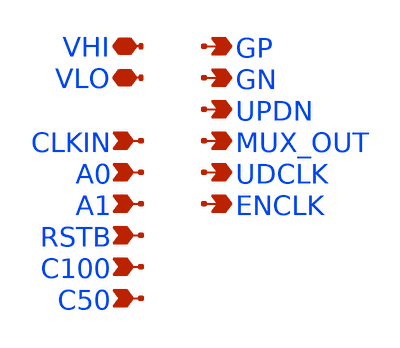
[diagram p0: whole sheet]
** sch_path: xschem/twcon_PEX.sch
**.subckt twcon_PEX VHI VLO UPDN CLKIN A0 A1 RSTB C100 C50 GP GN MUX_OUT UDCLK ENCLK
*.iopin VHI
*.iopin VLO
*.opin UPDN
*.ipin CLKIN
*.ipin A0
*.ipin A1
*.ipin RSTB
*.ipin C100
*.ipin C50
*.opin GP
*.opin GN
*.opin MUX_OUT
*.opin UDCLK
*.opin ENCLK
**** begin user architecture code

* NGSPICE file created from twcon.ext - technology: sky130A

* NGSPICE file created from twcon.ext - technology: sky130A

.subckt sky130_fd_sc_hs__decap_8 VGND VPWR VNB VPB
X0 VPWR VGND VPWR VPB sky130_fd_pr__pfet_01v8 ad=8.35e+11p pd=7.67e+06u as=0p ps=0u w=1e+06u
+ l=1e+06u
X1 VPWR VGND VPWR VPB sky130_fd_pr__pfet_01v8 ad=0p pd=0u as=0p ps=0u w=1e+06u l=1e+06u
X2 VGND VPWR VGND VNB sky130_fd_pr__nfet_01v8_lvt ad=3.465e+11p pd=4.17e+06u as=0p ps=0u w=420000u
+ l=1e+06u
X3 VGND VPWR VGND VNB sky130_fd_pr__nfet_01v8_lvt ad=0p pd=0u as=0p ps=0u w=420000u l=1e+06u
.ends

.subckt tcap_50f C S VLO
X0 a_173_157# C sky130_fd_pr__cap_mim_m3_2 l=1.6e+06u w=7.85e+06u
X1 a_173_157# S VLO VLO sky130_fd_pr__nfet_01v8 ad=5.8e+11p pd=4.58e+06u as=5.8e+11p ps=4.58e+06u
+ w=2e+06u l=150000u
X2 C a_173_157# sky130_fd_pr__cap_mim_m3_1 l=1.6e+06u w=7.85e+06u
.ends

.subckt sky130_fd_sc_hs__mux2_1 A0 A1 S VGND VPWR X VNB VPB
X0 VGND a_27_112# a_443_74# VNB sky130_fd_pr__nfet_01v8_lvt ad=7.0725e+11p pd=4.91e+06u
+ as=5.994e+11p ps=3.1e+06u w=740000u l=150000u
X1 VPWR S a_27_112# VPB sky130_fd_pr__pfet_01v8 ad=8.82e+11p pd=5.95e+06u as=2.478e+11p ps=2.27e+06u
+ w=840000u l=150000u
X2 X a_304_74# VPWR VPB sky130_fd_pr__pfet_01v8 ad=3.304e+11p pd=2.83e+06u as=0p ps=0u w=1.12e+06u
+ l=150000u
X3 VPWR a_27_112# a_524_368# VPB sky130_fd_pr__pfet_01v8 ad=0p pd=0u as=4.2e+11p ps=2.84e+06u
+ w=1e+06u l=150000u
X4 a_304_74# A1 a_226_74# VNB sky130_fd_pr__nfet_01v8_lvt ad=4.033e+11p pd=2.57e+06u as=1.776e+11p
+ ps=1.96e+06u w=740000u l=150000u
X5 X a_304_74# VGND VNB sky130_fd_pr__nfet_01v8_lvt ad=2.109e+11p pd=2.05e+06u as=0p ps=0u w=740000u
+ l=150000u
X6 a_223_368# S VPWR VPB sky130_fd_pr__pfet_01v8 ad=8.15e+11p pd=3.63e+06u as=0p ps=0u w=1e+06u
+ l=150000u
X7 a_304_74# A0 a_223_368# VPB sky130_fd_pr__pfet_01v8 ad=3.9e+11p pd=2.78e+06u as=0p ps=0u w=1e+06u
+ l=150000u
X8 a_443_74# A0 a_304_74# VNB sky130_fd_pr__nfet_01v8_lvt ad=0p pd=0u as=0p ps=0u w=740000u
+ l=150000u
X9 a_524_368# A1 a_304_74# VPB sky130_fd_pr__pfet_01v8 ad=0p pd=0u as=0p ps=0u w=1e+06u l=150000u
X10 a_226_74# S VGND VNB sky130_fd_pr__nfet_01v8_lvt ad=0p pd=0u as=0p ps=0u w=740000u l=150000u
X11 VGND S a_27_112# VNB sky130_fd_pr__nfet_01v8_lvt ad=0p pd=0u as=1.5675e+11p ps=1.67e+06u
+ w=550000u l=150000u
.ends

.subckt sky130_fd_sc_hs__decap_4 VGND VPWR VNB VPB
X0 VPWR VGND VPWR VPB sky130_fd_pr__pfet_01v8 ad=5.6e+11p pd=5.12e+06u as=0p ps=0u w=1e+06u l=1e+06u
X1 VGND VPWR VGND VNB sky130_fd_pr__nfet_01v8_lvt ad=2.31e+11p pd=2.78e+06u as=0p ps=0u w=420000u
+ l=1e+06u
.ends

.subckt tcap_100f C S VLO
X0 a_173_157# C sky130_fd_pr__cap_mim_m3_2 l=1.6e+06u w=1.57e+07u
X1 a_173_157# S VLO VLO sky130_fd_pr__nfet_01v8 ad=5.8e+11p pd=4.58e+06u as=5.8e+11p ps=4.58e+06u
+ w=2e+06u l=150000u
X2 C a_173_157# sky130_fd_pr__cap_mim_m3_1 l=1.6e+06u w=1.57e+07u
.ends

.subckt sky130_fd_sc_hs__sdfbbn_2 CLK_N D RESET_B SCD SCE SET_B VGND VPWR Q Q_N VNB  VPB
X0 a_1997_82# a_868_368# a_1986_424# VPB sky130_fd_pr__pfet_01v8 ad=2.856e+11p pd=2.45e+06u
+ as=2.016e+11p ps=2.16e+06u w=840000u l=150000u
X1 a_1185_125# a_1007_366# VGND VNB sky130_fd_pr__nfet_01v8_lvt ad=8.82e+10p pd=1.26e+06u
+ as=2.86405e+12p ps=2.37e+07u w=420000u l=150000u
X2 a_2452_74# SET_B VGND VNB sky130_fd_pr__nfet_01v8_lvt ad=5.7435e+11p pd=4.64e+06u as=0p ps=0u
+ w=740000u l=150000u
X3 a_1070_464# a_1007_366# VPWR VPB sky130_fd_pr__pfet_01v8 ad=1.134e+11p pd=1.38e+06u
+ as=4.12873e+12p ps=3.022e+07u w=420000u l=150000u
X4 a_363_119# D a_197_119# VNB sky130_fd_pr__nfet_01v8_lvt ad=1.008e+11p pd=1.32e+06u as=4.347e+11p
+ ps=3.75e+06u w=420000u l=150000u
X5 VGND a_2216_410# Q_N VNB sky130_fd_pr__nfet_01v8_lvt ad=0p pd=0u as=2.072e+11p ps=2.04e+06u
+ w=740000u l=150000u
X6 VGND a_2216_410# a_3272_94# VNB sky130_fd_pr__nfet_01v8_lvt ad=0p pd=0u as=1.824e+11p
+ ps=1.85e+06u w=640000u l=150000u
X7 a_119_119# SCD VGND VNB sky130_fd_pr__nfet_01v8_lvt ad=1.008e+11p pd=1.32e+06u as=0p ps=0u
+ w=420000u l=150000u
X8 VGND SET_B a_1473_73# VNB sky130_fd_pr__nfet_01v8_lvt ad=0p pd=0u as=6.0335e+11p ps=4.55e+06u
+ w=550000u l=150000u
X9 a_2247_82# a_868_368# a_1997_82# VNB sky130_fd_pr__nfet_01v8_lvt ad=1.008e+11p pd=1.32e+06u
+ as=4.945e+11p ps=3.3e+06u w=420000u l=150000u
X10 VGND CLK_N a_688_98# VNB sky130_fd_pr__nfet_01v8_lvt ad=0p pd=0u as=2.109e+11p ps=2.05e+06u
+ w=740000u l=150000u
X11 a_868_368# a_688_98# VGND VNB sky130_fd_pr__nfet_01v8_lvt ad=2.109e+11p pd=2.05e+06u as=0p ps=0u
+ w=740000u l=150000u
X12 VPWR a_3272_94# Q VPB sky130_fd_pr__pfet_01v8 ad=0p pd=0u as=3.36e+11p ps=2.84e+06u w=1.12e+06u
+ l=150000u
X13 a_2452_74# a_1997_82# a_2216_410# VNB sky130_fd_pr__nfet_01v8_lvt ad=0p pd=0u as=2.072e+11p
+ ps=2.04e+06u w=740000u l=150000u
X14 VPWR SCD a_27_464# VPB sky130_fd_pr__pfet_01v8 ad=0p pd=0u as=3.776e+11p ps=3.74e+06u w=640000u
+ l=150000u
X15 Q a_3272_94# VPWR VPB sky130_fd_pr__pfet_01v8 ad=0p pd=0u as=0p ps=0u w=1.12e+06u l=150000u
X16 a_1986_424# a_1007_366# VPWR VPB sky130_fd_pr__pfet_01v8 ad=0p pd=0u as=0p ps=0u w=840000u
+ l=150000u
X17 VPWR a_2216_410# a_2171_508# VPB sky130_fd_pr__pfet_01v8 ad=0p pd=0u as=1.008e+11p ps=1.32e+06u
+ w=420000u l=150000u
X18 a_2216_410# a_1997_82# a_2556_392# VPB sky130_fd_pr__pfet_01v8 ad=5.9e+11p pd=5.18e+06u
+ as=2.7e+11p ps=2.54e+06u w=1e+06u l=150000u
X19 a_341_410# SCE VPWR VPB sky130_fd_pr__pfet_01v8 ad=1.888e+11p pd=1.87e+06u as=0p ps=0u w=640000u
+ l=150000u
X20 a_1007_366# a_1154_464# a_1473_73# VNB sky130_fd_pr__nfet_01v8_lvt ad=1.54e+11p pd=1.66e+06u
+ as=0p ps=0u w=550000u l=150000u
X21 VPWR SET_B a_2216_410# VPB sky130_fd_pr__pfet_01v8 ad=0p pd=0u as=0p ps=0u w=1e+06u l=150000u
X22 VGND a_3272_94# Q VNB sky130_fd_pr__nfet_01v8_lvt ad=0p pd=0u as=2.072e+11p ps=2.04e+06u
+ w=740000u l=150000u
X23 VPWR a_1643_257# a_1592_424# VPB sky130_fd_pr__pfet_01v8 ad=0p pd=0u as=2.268e+11p ps=2.22e+06u
+ w=840000u l=150000u
X24 a_2171_508# a_688_98# a_1997_82# VPB sky130_fd_pr__pfet_01v8 ad=0p pd=0u as=0p ps=0u w=420000u
+ l=150000u
X25 a_1997_82# a_688_98# a_1902_125# VNB sky130_fd_pr__nfet_01v8_lvt ad=0p pd=0u as=2.16375e+11p
+ ps=2.18e+06u w=550000u l=150000u
X26 a_2556_392# a_1643_257# VPWR VPB sky130_fd_pr__pfet_01v8 ad=0p pd=0u as=0p ps=0u w=1e+06u
+ l=150000u
X27 a_1592_424# a_1154_464# a_1007_366# VPB sky130_fd_pr__pfet_01v8 ad=0p pd=0u as=9.954e+11p
+ ps=5.73e+06u w=840000u l=150000u
X28 a_1007_366# SET_B VPWR VPB sky130_fd_pr__pfet_01v8 ad=0p pd=0u as=0p ps=0u w=840000u l=150000u
X29 VPWR RESET_B a_1643_257# VPB sky130_fd_pr__pfet_01v8 ad=0p pd=0u as=1.888e+11p ps=1.87e+06u
+ w=640000u l=150000u
X30 VPWR a_2216_410# Q_N VPB sky130_fd_pr__pfet_01v8 ad=0p pd=0u as=3.36e+11p ps=2.84e+06u
+ w=1.12e+06u l=150000u
X31 a_2216_410# a_1643_257# a_2452_74# VNB sky130_fd_pr__nfet_01v8_lvt ad=0p pd=0u as=0p ps=0u
+ w=740000u l=150000u
X32 a_197_119# SCE a_119_119# VNB sky130_fd_pr__nfet_01v8_lvt ad=0p pd=0u as=0p ps=0u w=420000u
+ l=150000u
X33 Q_N a_2216_410# VPWR VPB sky130_fd_pr__pfet_01v8 ad=0p pd=0u as=0p ps=0u w=1.12e+06u l=150000u
X34 VGND a_2216_410# a_2247_82# VNB sky130_fd_pr__nfet_01v8_lvt ad=0p pd=0u as=0p ps=0u w=420000u
+ l=150000u
X35 a_27_464# a_341_410# a_197_119# VPB sky130_fd_pr__pfet_01v8 ad=0p pd=0u as=4.128e+11p
+ ps=3.85e+06u w=640000u l=150000u
X36 a_1473_73# a_1643_257# a_1007_366# VNB sky130_fd_pr__nfet_01v8_lvt ad=0p pd=0u as=0p ps=0u
+ w=550000u l=150000u
X37 a_197_119# D a_206_464# VPB sky130_fd_pr__pfet_01v8 ad=0p pd=0u as=1.536e+11p ps=1.76e+06u
+ w=640000u l=150000u
X38 a_1154_464# a_688_98# a_1185_125# VNB sky130_fd_pr__nfet_01v8_lvt ad=1.281e+11p pd=1.45e+06u
+ as=0p ps=0u w=420000u l=150000u
X39 a_1902_125# a_1007_366# VGND VNB sky130_fd_pr__nfet_01v8_lvt ad=0p pd=0u as=0p ps=0u w=550000u
+ l=150000u
X40 Q a_3272_94# VGND VNB sky130_fd_pr__nfet_01v8_lvt ad=0p pd=0u as=0p ps=0u w=740000u l=150000u
X41 a_197_119# a_688_98# a_1154_464# VPB sky130_fd_pr__pfet_01v8 ad=0p pd=0u as=2.266e+11p
+ ps=2.05e+06u w=640000u l=150000u
X42 VPWR a_2216_410# a_3272_94# VPB sky130_fd_pr__pfet_01v8 ad=0p pd=0u as=2.9e+11p ps=2.58e+06u
+ w=1e+06u l=150000u
X43 VGND RESET_B a_1643_257# VNB sky130_fd_pr__nfet_01v8_lvt ad=0p pd=0u as=1.176e+11p ps=1.4e+06u
+ w=420000u l=150000u
X44 a_868_368# a_688_98# VPWR VPB sky130_fd_pr__pfet_01v8 ad=3.304e+11p pd=2.83e+06u as=0p ps=0u
+ w=1.12e+06u l=150000u
X45 a_197_119# a_868_368# a_1154_464# VNB sky130_fd_pr__nfet_01v8_lvt ad=0p pd=0u as=0p ps=0u
+ w=420000u l=150000u
X46 a_206_464# SCE VPWR VPB sky130_fd_pr__pfet_01v8 ad=0p pd=0u as=0p ps=0u w=640000u l=150000u
X47 VPWR CLK_N a_688_98# VPB sky130_fd_pr__pfet_01v8 ad=0p pd=0u as=3.304e+11p ps=2.83e+06u
+ w=1.12e+06u l=150000u
X48 a_1154_464# a_868_368# a_1070_464# VPB sky130_fd_pr__pfet_01v8 ad=0p pd=0u as=0p ps=0u w=420000u
+ l=150000u
X49 VGND a_341_410# a_363_119# VNB sky130_fd_pr__nfet_01v8_lvt ad=0p pd=0u as=0p ps=0u w=420000u
+ l=150000u
X50 a_341_410# SCE VGND VNB sky130_fd_pr__nfet_01v8_lvt ad=1.197e+11p pd=1.41e+06u as=0p ps=0u
+ w=420000u l=150000u
X51 Q_N a_2216_410# VGND VNB sky130_fd_pr__nfet_01v8_lvt ad=0p pd=0u as=0p ps=0u w=740000u l=150000u
.ends

.subckt sky130_fd_sc_hs__inv_1 A VGND VPWR Y VNB VPB
X0 Y A VPWR VPB sky130_fd_pr__pfet_01v8 ad=3.304e+11p pd=2.83e+06u as=3.864e+11p ps=2.93e+06u
+ w=1.12e+06u l=150000u
X1 Y A VGND VNB sky130_fd_pr__nfet_01v8_lvt ad=2.109e+11p pd=2.05e+06u as=2.627e+11p ps=2.19e+06u
+ w=740000u l=150000u
.ends

.subckt sky130_fd_sc_hs__nand2_1 A B VGND VPWR Y VNB VPB
X0 a_117_74# B VGND VNB sky130_fd_pr__nfet_01v8_lvt ad=1.776e+11p pd=1.96e+06u as=2.109e+11p
+ ps=2.05e+06u w=740000u l=150000u
X1 VPWR A Y VPB sky130_fd_pr__pfet_01v8 ad=6.384e+11p pd=5.62e+06u as=3.36e+11p ps=2.84e+06u
+ w=1.12e+06u l=150000u
X2 Y A a_117_74# VNB sky130_fd_pr__nfet_01v8_lvt ad=2.109e+11p pd=2.05e+06u as=0p ps=0u w=740000u
+ l=150000u
X3 Y B VPWR VPB sky130_fd_pr__pfet_01v8 ad=0p pd=0u as=0p ps=0u w=1.12e+06u l=150000u
.ends

.subckt sky130_fd_pr__res_xhigh_po_1p41_GKKP9B a_n141_n482# a_n141_50# VSUBS
X0 a_n141_n482# a_n141_50# VSUBS sky130_fd_pr__res_xhigh_po_1p41 l=500000u
.ends

.subckt twcon_tdly C A Y sky130_fd_sc_hs__inv_1_0/VGND VSUBS sky130_fd_sc_hs__inv_1_0/VPWR
+  sky130_fd_sc_hs__inv_1_0/VPB
Xsky130_fd_sc_hs__inv_1_0 A sky130_fd_sc_hs__inv_1_0/VGND sky130_fd_sc_hs__inv_1_0/VPWR
+  sky130_fd_sc_hs__inv_1_0/Y VSUBS sky130_fd_sc_hs__inv_1_0/VPB sky130_fd_sc_hs__inv_1
Xsky130_fd_sc_hs__nand2_1_2 A C sky130_fd_sc_hs__inv_1_0/VGND sky130_fd_sc_hs__inv_1_0/VPWR  Y VSUBS
+ sky130_fd_sc_hs__inv_1_0/VPB sky130_fd_sc_hs__nand2_1
Xsky130_fd_pr__res_xhigh_po_1p41_GKKP9B_0 sky130_fd_sc_hs__inv_1_0/Y C VSUBS
+ sky130_fd_pr__res_xhigh_po_1p41_GKKP9B
.ends

.subckt sky130_fd_sc_hs__nand2_4 A B VGND VPWR Y VNB VPB
X0 Y A a_27_74# VNB sky130_fd_pr__nfet_01v8_lvt ad=5.365e+11p pd=4.41e+06u as=1.1581e+12p
+ ps=1.053e+07u w=740000u l=150000u
X1 Y B VPWR VPB sky130_fd_pr__pfet_01v8 ad=2.7496e+12p pd=9.39e+06u as=1.1144e+12p ps=8.71e+06u
+ w=1.12e+06u l=150000u
X2 VPWR A Y VPB sky130_fd_pr__pfet_01v8 ad=0p pd=0u as=0p ps=0u w=1.12e+06u l=150000u
X3 Y A a_27_74# VNB sky130_fd_pr__nfet_01v8_lvt ad=0p pd=0u as=0p ps=0u w=740000u l=150000u
X4 Y A VPWR VPB sky130_fd_pr__pfet_01v8 ad=0p pd=0u as=0p ps=0u w=1.12e+06u l=150000u
X5 VGND B a_27_74# VNB sky130_fd_pr__nfet_01v8_lvt ad=4.144e+11p pd=4.08e+06u as=0p ps=0u w=740000u
+ l=150000u
X6 a_27_74# A Y VNB sky130_fd_pr__nfet_01v8_lvt ad=0p pd=0u as=0p ps=0u w=740000u l=150000u
X7 VPWR B Y VPB sky130_fd_pr__pfet_01v8 ad=0p pd=0u as=0p ps=0u w=1.12e+06u l=150000u
X8 a_27_74# B VGND VNB sky130_fd_pr__nfet_01v8_lvt ad=0p pd=0u as=0p ps=0u w=740000u l=150000u
X9 a_27_74# A Y VNB sky130_fd_pr__nfet_01v8_lvt ad=0p pd=0u as=0p ps=0u w=740000u l=150000u
X10 a_27_74# B VGND VNB sky130_fd_pr__nfet_01v8_lvt ad=0p pd=0u as=0p ps=0u w=740000u l=150000u
X11 VGND B a_27_74# VNB sky130_fd_pr__nfet_01v8_lvt ad=0p pd=0u as=0p ps=0u w=740000u l=150000u
.ends

.subckt sky130_fd_sc_hs__inv_2 A VGND VPWR Y VNB VPB
X0 Y A VGND VNB sky130_fd_pr__nfet_01v8_lvt ad=2.072e+11p pd=2.04e+06u as=4.218e+11p ps=4.1e+06u
+ w=740000u l=150000u
X1 VPWR A Y VPB sky130_fd_pr__pfet_01v8 ad=6.384e+11p pd=5.62e+06u as=3.36e+11p ps=2.84e+06u
+ w=1.12e+06u l=150000u
X2 VGND A Y VNB sky130_fd_pr__nfet_01v8_lvt ad=0p pd=0u as=0p ps=0u w=740000u l=150000u
X3 Y A VPWR VPB sky130_fd_pr__pfet_01v8 ad=0p pd=0u as=0p ps=0u w=1.12e+06u l=150000u
.ends

.subckt sky130_fd_sc_hs__and2_4 A B VGND VPWR X VNB VPB
X0 X a_83_269# VPWR VPB sky130_fd_pr__pfet_01v8 ad=6.944e+11p pd=5.72e+06u as=1.58705e+12p
+ ps=1.328e+07u w=1.12e+06u l=150000u
X1 a_83_269# B VPWR VPB sky130_fd_pr__pfet_01v8 ad=5.25e+11p pd=4.61e+06u as=0p ps=0u w=840000u
+ l=150000u
X2 a_83_269# A a_504_119# VNB sky130_fd_pr__nfet_01v8_lvt ad=2.08e+11p pd=1.93e+06u as=3.872e+11p
+ ps=3.77e+06u w=640000u l=150000u
X3 VPWR a_83_269# X VPB sky130_fd_pr__pfet_01v8 ad=0p pd=0u as=0p ps=0u w=1.12e+06u l=150000u
X4 VGND a_83_269# X VNB sky130_fd_pr__nfet_01v8_lvt ad=8.594e+11p pd=8.14e+06u as=5.254e+11p
+ ps=4.38e+06u w=740000u l=150000u
X5 X a_83_269# VGND VNB sky130_fd_pr__nfet_01v8_lvt ad=0p pd=0u as=0p ps=0u w=740000u l=150000u
X6 X a_83_269# VPWR VPB sky130_fd_pr__pfet_01v8 ad=0p pd=0u as=0p ps=0u w=1.12e+06u l=150000u
X7 VPWR a_83_269# X VPB sky130_fd_pr__pfet_01v8 ad=0p pd=0u as=0p ps=0u w=1.12e+06u l=150000u
X8 VPWR B a_83_269# VPB sky130_fd_pr__pfet_01v8 ad=0p pd=0u as=0p ps=0u w=840000u l=150000u
X9 a_83_269# A VPWR VPB sky130_fd_pr__pfet_01v8 ad=0p pd=0u as=0p ps=0u w=840000u l=150000u
X10 VGND a_83_269# X VNB sky130_fd_pr__nfet_01v8_lvt ad=0p pd=0u as=0p ps=0u w=740000u l=150000u
X11 VPWR A a_83_269# VPB sky130_fd_pr__pfet_01v8 ad=0p pd=0u as=0p ps=0u w=840000u l=150000u
X12 VGND B a_504_119# VNB sky130_fd_pr__nfet_01v8_lvt ad=0p pd=0u as=0p ps=0u w=640000u l=150000u
X13 a_504_119# A a_83_269# VNB sky130_fd_pr__nfet_01v8_lvt ad=0p pd=0u as=0p ps=0u w=640000u
+ l=150000u
X14 X a_83_269# VGND VNB sky130_fd_pr__nfet_01v8_lvt ad=0p pd=0u as=0p ps=0u w=740000u l=150000u
X15 a_504_119# B VGND VNB sky130_fd_pr__nfet_01v8_lvt ad=0p pd=0u as=0p ps=0u w=640000u l=150000u
.ends

.subckt twcon UPDN CLKIN A0 A1 RSTB VHI VLO C100 C50 MUX_OUT ENCLK GN GP
Xsky130_fd_sc_hs__decap_8_0 VLO VHI VLO VHI sky130_fd_sc_hs__decap_8
Xtcap_50f_0 tcap_50f_0/C C100 VLO tcap_50f
Xsky130_fd_sc_hs__decap_8_2 VLO VHI VLO VHI sky130_fd_sc_hs__decap_8
Xsky130_fd_sc_hs__decap_8_3 VLO VHI VLO VHI sky130_fd_sc_hs__decap_8
Xtcap_50f_3 tcap_50f_3/C C100 VLO tcap_50f
Xsky130_fd_sc_hs__decap_8_4 VLO VHI VLO VHI sky130_fd_sc_hs__decap_8
Xtcap_50f_2 tcap_50f_2/C C50 VLO tcap_50f
Xsky130_fd_sc_hs__mux2_1_1 twcon_tdly_1/Y twcon_tdly_2/Y sky130_fd_sc_hs__mux2_1_1/S  VLO VHI
+ MUX_OUT VLO VHI sky130_fd_sc_hs__mux2_1
Xsky130_fd_sc_hs__decap_8_6 VLO VHI VLO VHI sky130_fd_sc_hs__decap_8
Xsky130_fd_sc_hs__decap_4_0 VLO VHI VLO VHI sky130_fd_sc_hs__decap_4
Xsky130_fd_sc_hs__decap_8_7 VLO VHI VLO VHI sky130_fd_sc_hs__decap_8
Xtcap_100f_0 tcap_50f_0/C C50 VLO tcap_100f
Xtcap_100f_2 tcap_50f_2/C C100 VLO tcap_100f
Xtcap_100f_3 tcap_50f_3/C C50 VLO tcap_100f
Xsky130_fd_sc_hs__sdfbbn_2_0 ENCLK VHI MUX_OUT VLO VLO VHI VLO VHI sky130_fd_sc_hs__and2_4_0/B
+  sky130_fd_sc_hs__sdfbbn_2_0/Q_N VLO VHI sky130_fd_sc_hs__sdfbbn_2
Xsky130_fd_sc_hs__sdfbbn_2_1 twcon_tdly_0/Y sky130_fd_sc_hs__mux2_1_1/S RSTB VLO VLO  VHI VLO VHI
+ UPDN sky130_fd_sc_hs__mux2_1_1/S VLO VHI sky130_fd_sc_hs__sdfbbn_2
Xtwcon_tdly_0 tcap_50f_2/C CLKIN twcon_tdly_0/Y VLO VLO VHI VHI twcon_tdly
Xtwcon_tdly_1 tcap_50f_0/C A0 twcon_tdly_1/Y VLO VLO VHI VHI twcon_tdly
Xtwcon_tdly_2 tcap_50f_3/C A1 twcon_tdly_2/Y VLO VLO VHI VHI twcon_tdly
Xsky130_fd_sc_hs__nand2_4_3 sky130_fd_sc_hs__and2_4_0/B UPDN VLO VHI GP VLO VHI
+ sky130_fd_sc_hs__nand2_4
Xsky130_fd_sc_hs__inv_2_1 CLKIN VLO VHI ENCLK VLO VHI sky130_fd_sc_hs__inv_2
Xsky130_fd_sc_hs__and2_4_0 sky130_fd_sc_hs__mux2_1_1/S sky130_fd_sc_hs__and2_4_0/B  VLO VHI GN VLO
+ VHI sky130_fd_sc_hs__and2_4
.ends



XDUT UPDN CLKIN A0 A1 RSTB VHI VLO C100 C50 MUX_OUT ENCLK GN GP twcon


**** end user architecture code
**.ends
.end
